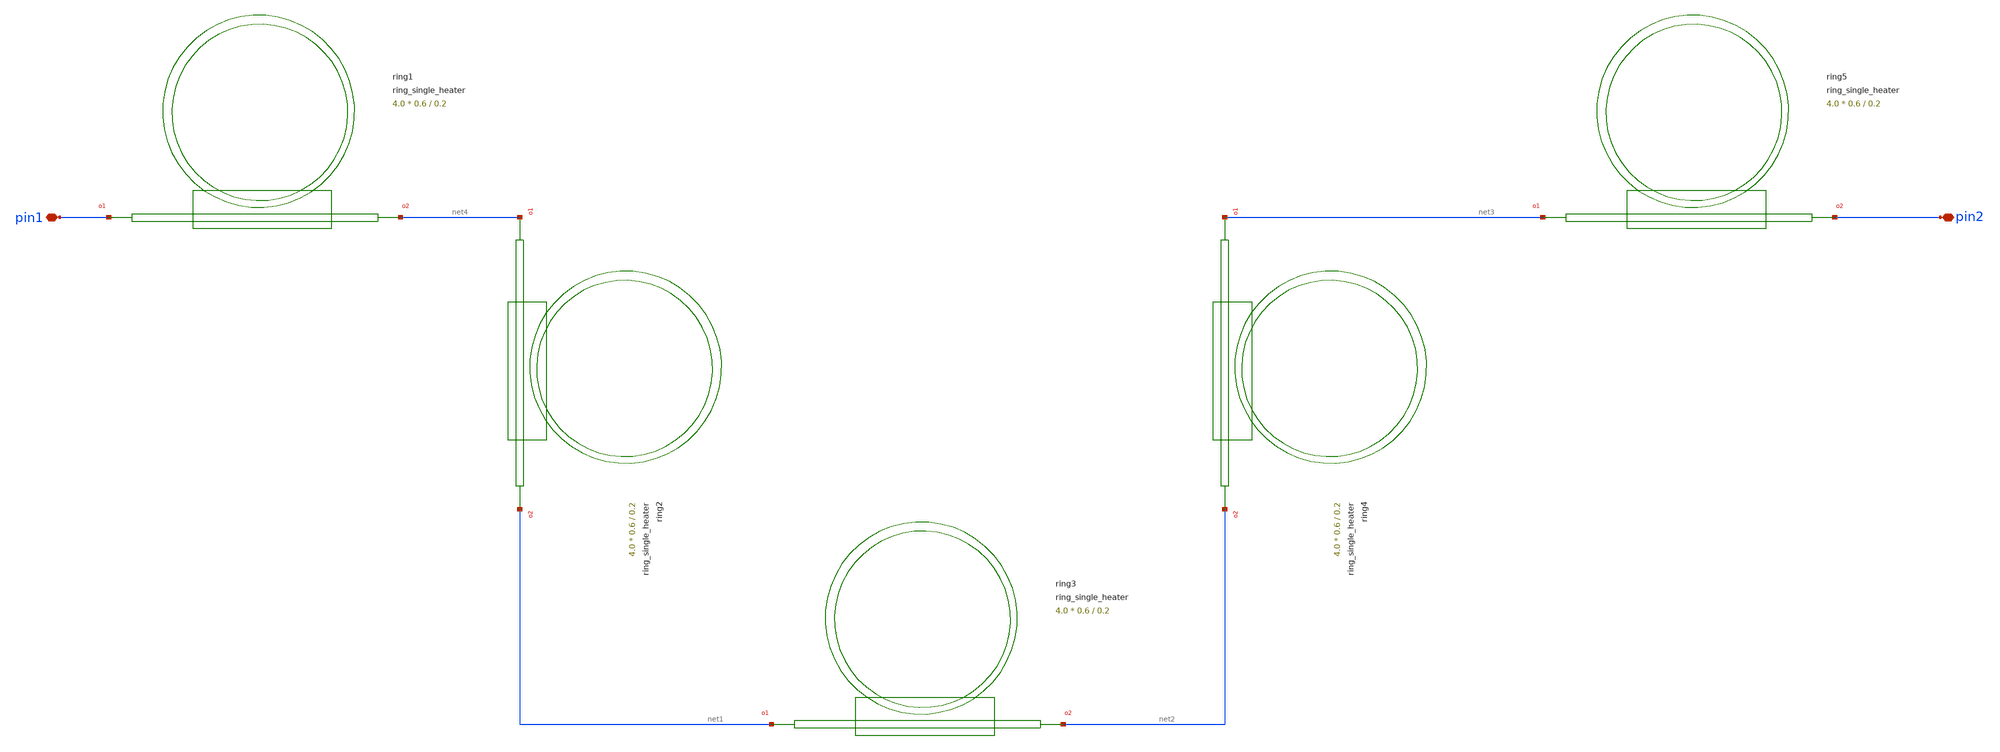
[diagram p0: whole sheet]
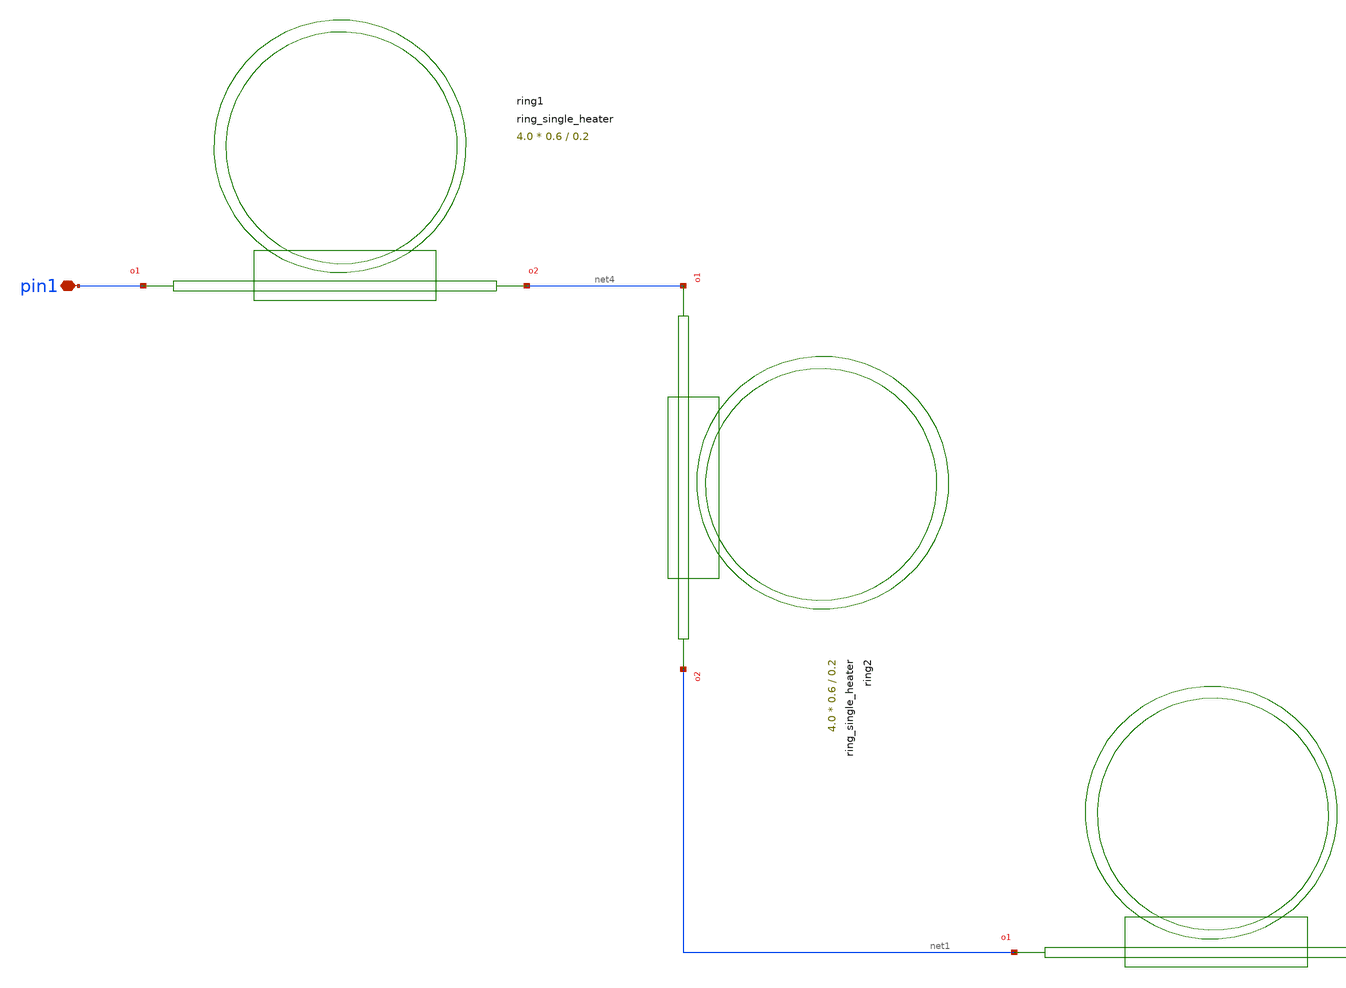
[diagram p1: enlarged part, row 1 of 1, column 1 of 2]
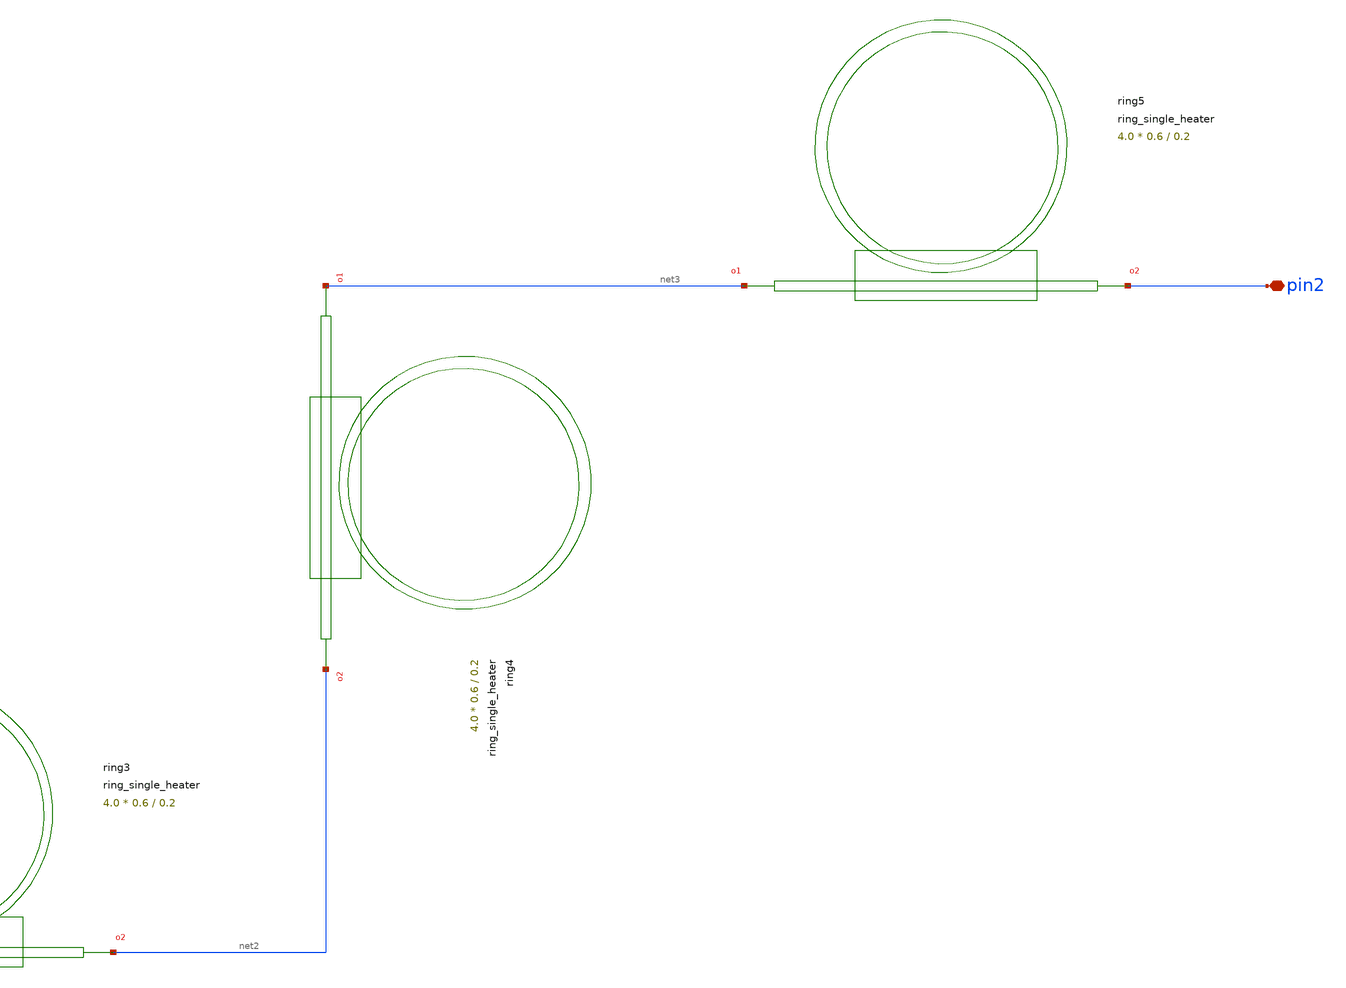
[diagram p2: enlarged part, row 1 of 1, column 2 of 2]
** sch_path: cells/xschem/tests/test_ring_single_heater.sch
* SPDX-FileCopyrightText: 2023 Mabrains Company
* Licensed under the GNU GENERAL PUBLIC License, Version 3.0 (the "License");
* you may not use this file except in compliance with the License.
* GNU GENERAL PUBLIC LICENSE
* Version 3, 29 June 2007
* This program is free software: you can redistribute it and/or modify
* it under the terms of the GNU General Public License as published
* by the Free Software Foundation, either 3 of the License, or
* (at your option) any later version.
* This program is distributed in the hope that it will be useful,
* but WITHOUT ANY WARRANTY; without even the implied warranty of
* MERCHANTABILITY or FITNESS FOR A PARTICULAR PURPOSE.  See the
* GNU General Public License for more details.
* You should have received a copy of the GNU General Public License
* along with this program.  If not, see <https://www.gnu.org/licenses/>.
* SPDX-License-Identifier: GPL-3.0
**.subckt test_ring_single_heater pin1 pin2
*.iopin pin1
*.iopin pin2
Pring1 pin1 net4 ring_single_heater gap=0.2 radius=10.0 length_x=4.0 length_y=0.6
Pring2 net4 net1 ring_single_heater gap=0.2 radius=10.0 length_x=4.0 length_y=0.6
Pring3 net1 net2 ring_single_heater gap=0.2 radius=10.0 length_x=4.0 length_y=0.6
Pring4 net3 net2 ring_single_heater gap=0.2 radius=10.0 length_x=4.0 length_y=0.6
Pring5 net3 pin2 ring_single_heater gap=0.2 radius=10.0 length_x=4.0 length_y=0.6
**.ends
.end
